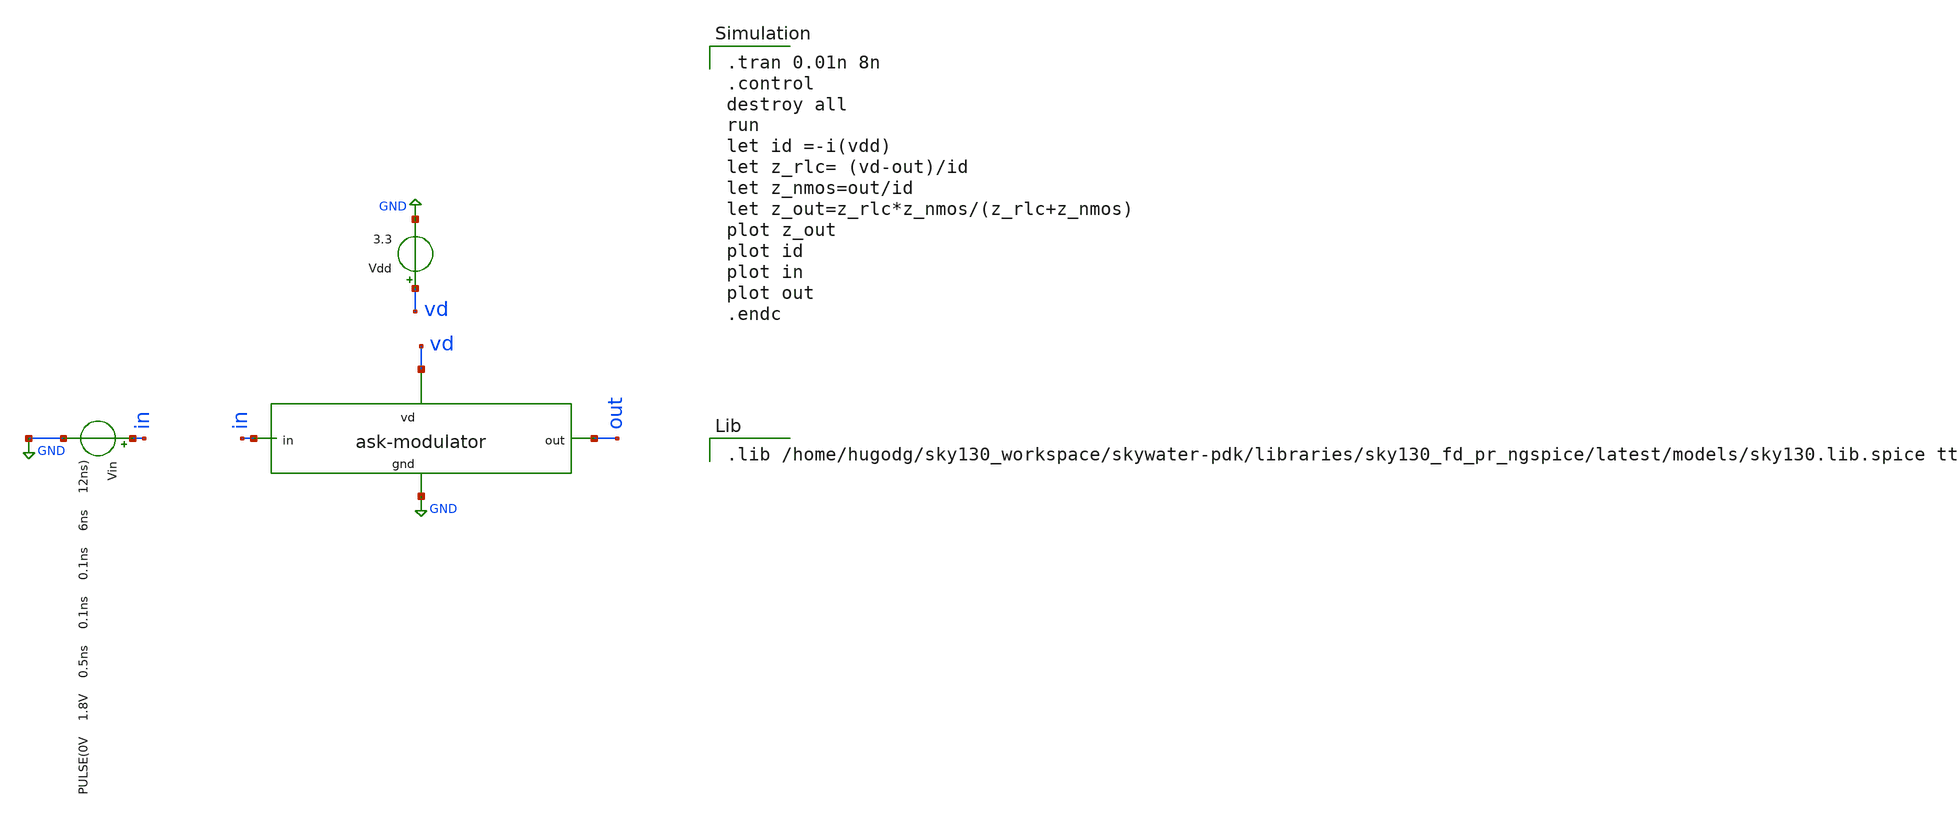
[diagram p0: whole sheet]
** sch_path: ask_modulator/xschem/ask-modulator_tb-tran.sch
**.subckt ask-modulator_tb-tran
Vdd vd GND 3.3
Vin in GND PULSE(0V 1.8V 0.5ns 0.1ns 0.1ns 6ns 12ns)
x1 vd out in GND ask-modulator
**** begin user architecture code

.tran 0.01n 8n
.control
destroy all
run
let id =-i(vdd)
let z_rlc= (vd-out)/id
let z_nmos=out/id
let z_out=z_rlc*z_nmos/(z_rlc+z_nmos)
plot z_out
plot id
plot in
plot out
.endc


.lib /home/hugodg/sky130_workspace/skywater-pdk/libraries/sky130_fd_pr_ngspice/latest/models/sky130.lib.spice tt

**** end user architecture code
**.ends

* expanding   symbol:  ask-modulator.sym # of pins=4
** sym_path: ask_modulator/xschem/ask-modulator.sym
** sch_path: ask_modulator/xschem/ask-modulator.sch
.subckt ask-modulator vd out in gnd
*.iopin gnd
*.ipin in
*.opin out
*.iopin vd
XM2 out in gnd gnd sky130_fd_pr__nfet_g5v0d10v5 L=1 W=21 nf=5 ad='int((nf+1)/2) * W/nf * 0.29' as='int((nf+2)/2) * W/nf * 0.29'
+ pd='2*int((nf+1)/2) * (W/nf + 0.29)' ps='2*int((nf+2)/2) * (W/nf + 0.29)' nrd='0.29 / W' nrs='0.29 / W'
+ sa=0 sb=0 sd=0 mult=1 m=1
L0 vd out 5.097n m=1
XC0 vd out sky130_fd_pr__cap_mim_m3_1 W=19.75 L=19.75 MF=1 m=1
XR0 out vd gnd sky130_fd_pr__res_high_po_5p73 L=0.5 mult=1 m=1
.ends

.GLOBAL GND
.end
